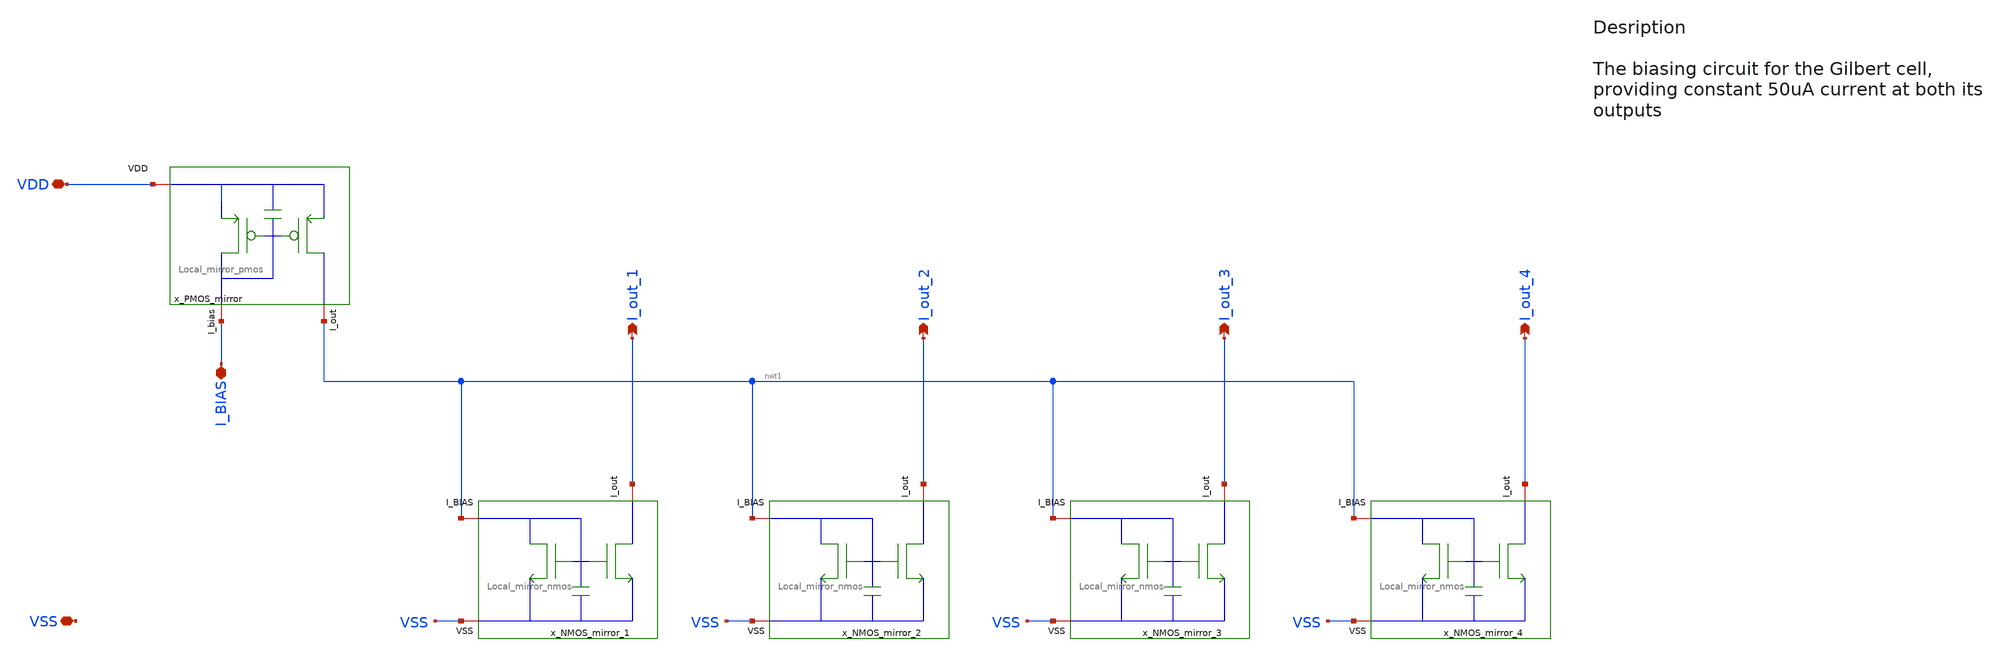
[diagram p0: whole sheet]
** sch_path: designs/libs/core_top/A5_Time_Transcenders/schematics/Biasing_network_with_local_mirros.sch
**.subckt Biasing_network_with_local_mirros VSS I_BIAS I_out_1 I_out_2 I_out_3 VDD I_out_4
*.iopin VSS
*.iopin I_BIAS
*.opin I_out_1
*.opin I_out_2
*.opin I_out_3
*.iopin VDD
*.opin I_out_4
x_PMOS_mirror VDD net1 I_BIAS Local_mirror_pmos w_ref=pmos_w_ref l_ref=pmos_l_ref w_mir=pmos_w_mir
+ l_mir=pmos_l_mir
x_NMOS_mirror_1 I_out_1 net1 VSS Local_mirror_nmos l_ref=nmos_l_ref_1 w_ref=nmos_w_ref_1
+ nf_ref=nmos_nf_ref_1 l_mir=nmos_l_mir_1 w_mir=nmos_w_mir_1 nf_mir=nmos_nf_mir_1
x_NMOS_mirror_2 I_out_2 net1 VSS Local_mirror_nmos l_ref=nmos_l_ref_2 w_ref=nmos_w_ref_2
+ nf_ref=nmos_nf_ref_2 l_mir=nmos_l_mir_2 w_mir=nmos_w_mir_2 nf_mir=nmos_nf_mir_2
x_NMOS_mirror_3 I_out_3 net1 VSS Local_mirror_nmos l_ref=nmos_l_ref_3 w_ref=nmos_w_ref_3
+ nf_ref=nmos_nf_ref_3 l_mir=nmos_l_mir_3 w_mir=nmos_w_mir_3 nf_mir=nmos_nf_mir_3
x_NMOS_mirror_4 I_out_4 net1 VSS Local_mirror_nmos l_ref=nmos_l_ref_4 w_ref=nmos_w_ref_4
+ nf_ref=nmos_nf_ref_4 l_mir=nmos_l_mir_4 w_mir=nmos_w_mir_4 nf_mir=nmos_nf_mir_4
**** begin user architecture code

.include $::180MCU_MODELS/design.ngspice
.lib $::180MCU_MODELS/sm141064.ngspice typical
.lib $::180MCU_MODELS/sm141064.ngspice mimcap_typical
.lib $::180MCU_MODELS/sm141064.ngspice cap_mim
.lib $::180MCU_MODELS/sm141064.ngspice res_typical




* let sets vectors to a plot, while set sets a variable, globally accessible in .control
.control

    * Set frequency and amplitude variables to proper values from within the control sequence
    save all

    op
    show

    write Biasing_network_sim.raw

    set appendwrite

    * Transient analysis to observe mixing operation
    tran 1p 10n


    write Biasing_network_sim.raw

.endc


**** end user architecture code
**.ends
.end
